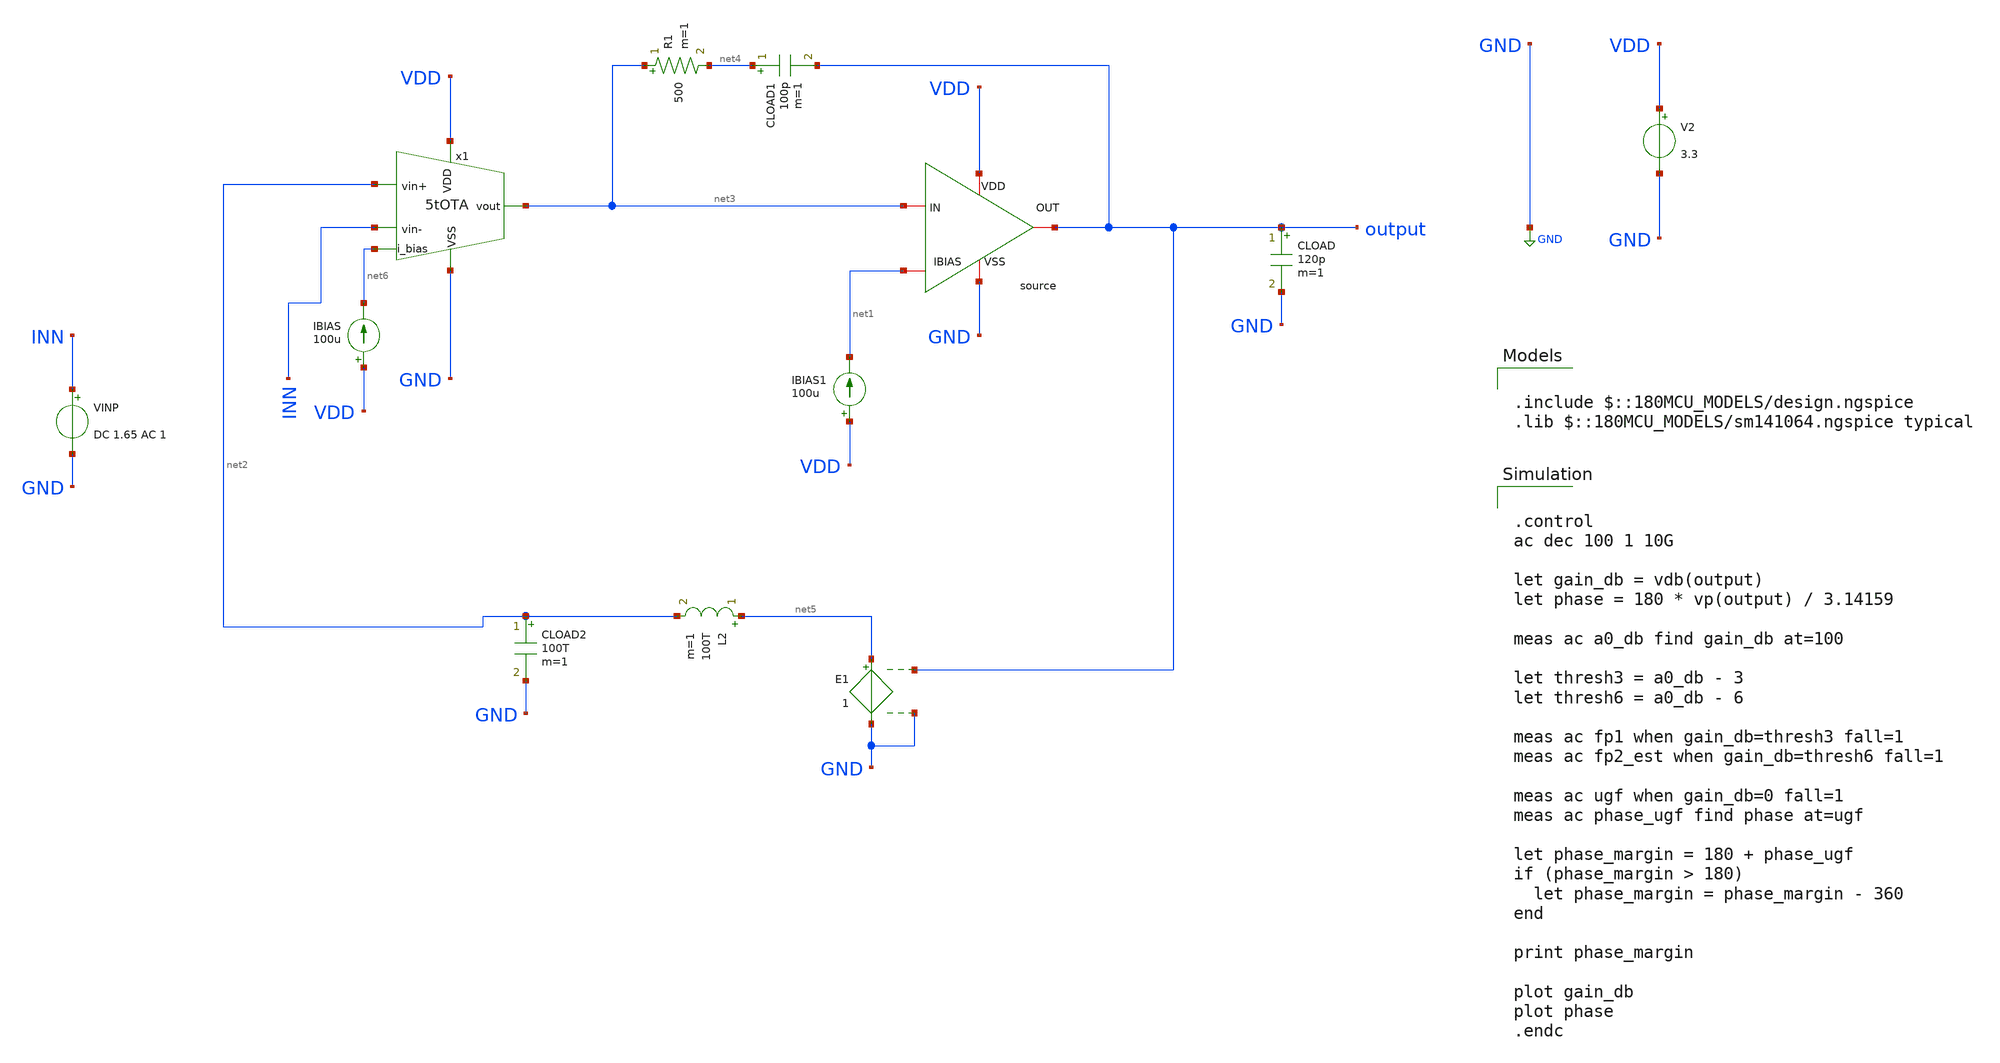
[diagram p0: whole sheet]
** sch_path: designs/libs/core_amps/two_stage_amps/5t_cs_ac_comp_tb.sch
**.subckt 5t_cs_ac_comp_tb
x2 VDD net3 net1 output GND cs_schematic
V2 VDD GND 3.3
IBIAS VDD net6 100u
IBIAS1 VDD net1 100u
CLOAD output GND 120p m=1
CLOAD1 net4 output 100p m=1
R1 net3 net4 500 m=1
VINP INN GND DC 1.65 AC 1
L2 net5 net2 100T m=1
CLOAD2 net2 GND 100T m=1
E1 net5 GND output GND 1
x1 VDD net3 net2 INN net6 GND 5tOTA
**** begin user architecture code

.include $::180MCU_MODELS/design.ngspice
.lib $::180MCU_MODELS/sm141064.ngspice typical



.control
ac dec 100 1 10G

let gain_db = vdb(output)
let phase = 180 * vp(output) / 3.14159

meas ac a0_db find gain_db at=100

let thresh3 = a0_db - 3
let thresh6 = a0_db - 6

meas ac fp1 when gain_db=thresh3 fall=1
meas ac fp2_est when gain_db=thresh6 fall=1

meas ac ugf when gain_db=0 fall=1
meas ac phase_ugf find phase at=ugf

let phase_margin = 180 + phase_ugf
if (phase_margin > 180)
  let phase_margin = phase_margin - 360
end

print phase_margin

plot gain_db
plot phase
.endc



**** end user architecture code
**.ends
.GLOBAL GND
.end
